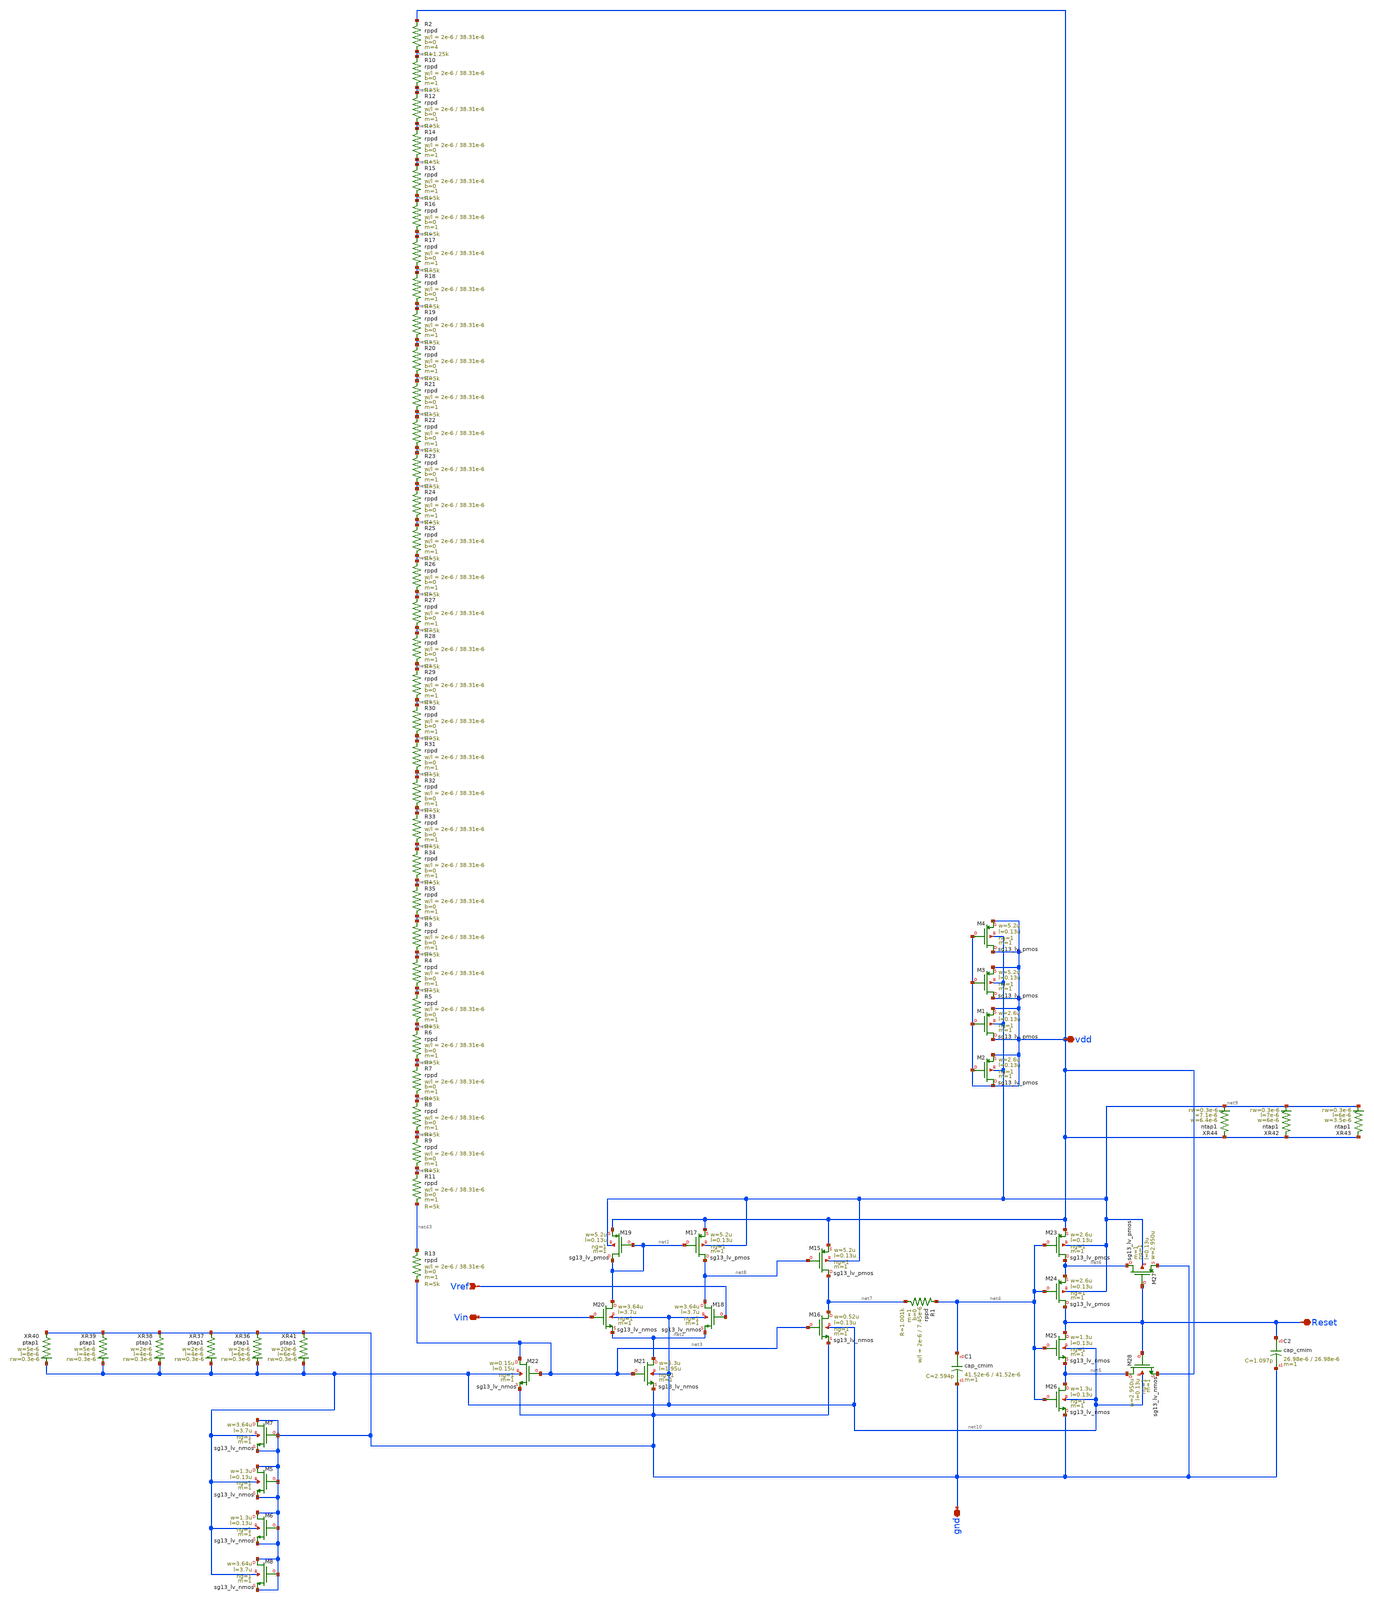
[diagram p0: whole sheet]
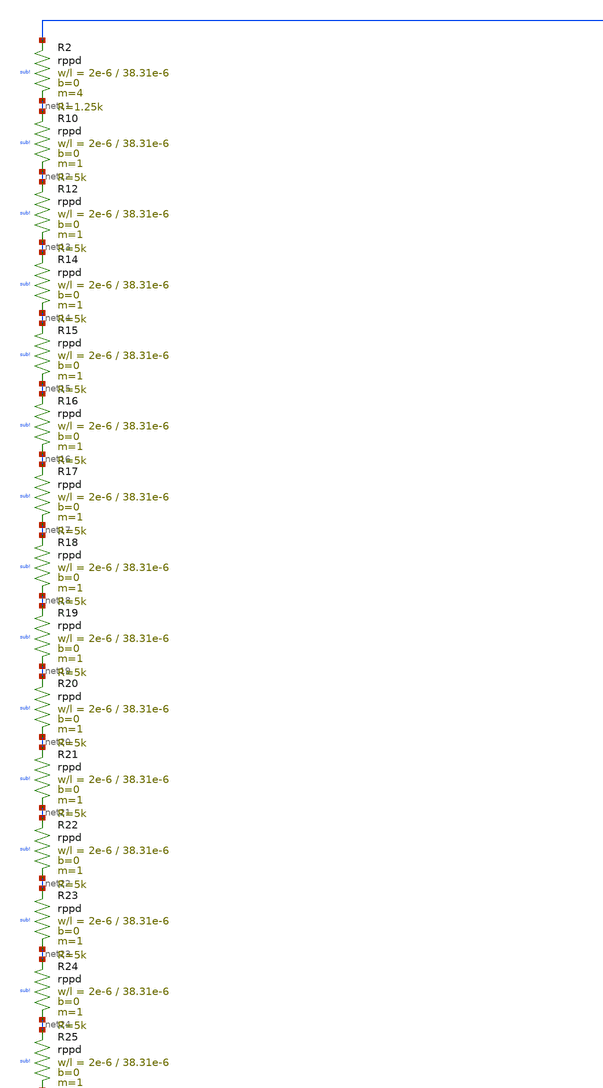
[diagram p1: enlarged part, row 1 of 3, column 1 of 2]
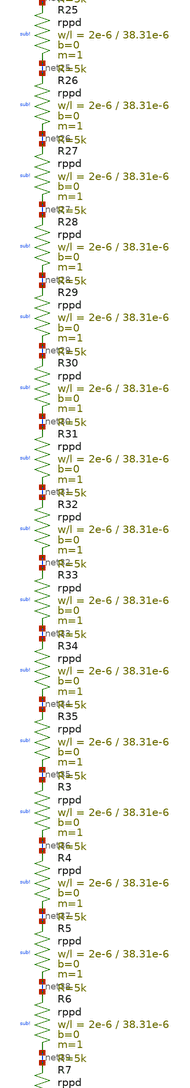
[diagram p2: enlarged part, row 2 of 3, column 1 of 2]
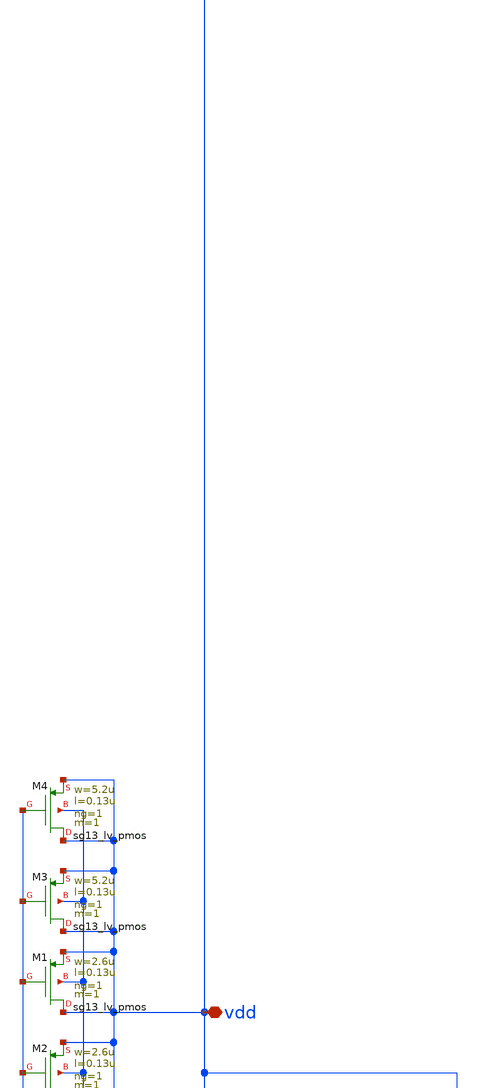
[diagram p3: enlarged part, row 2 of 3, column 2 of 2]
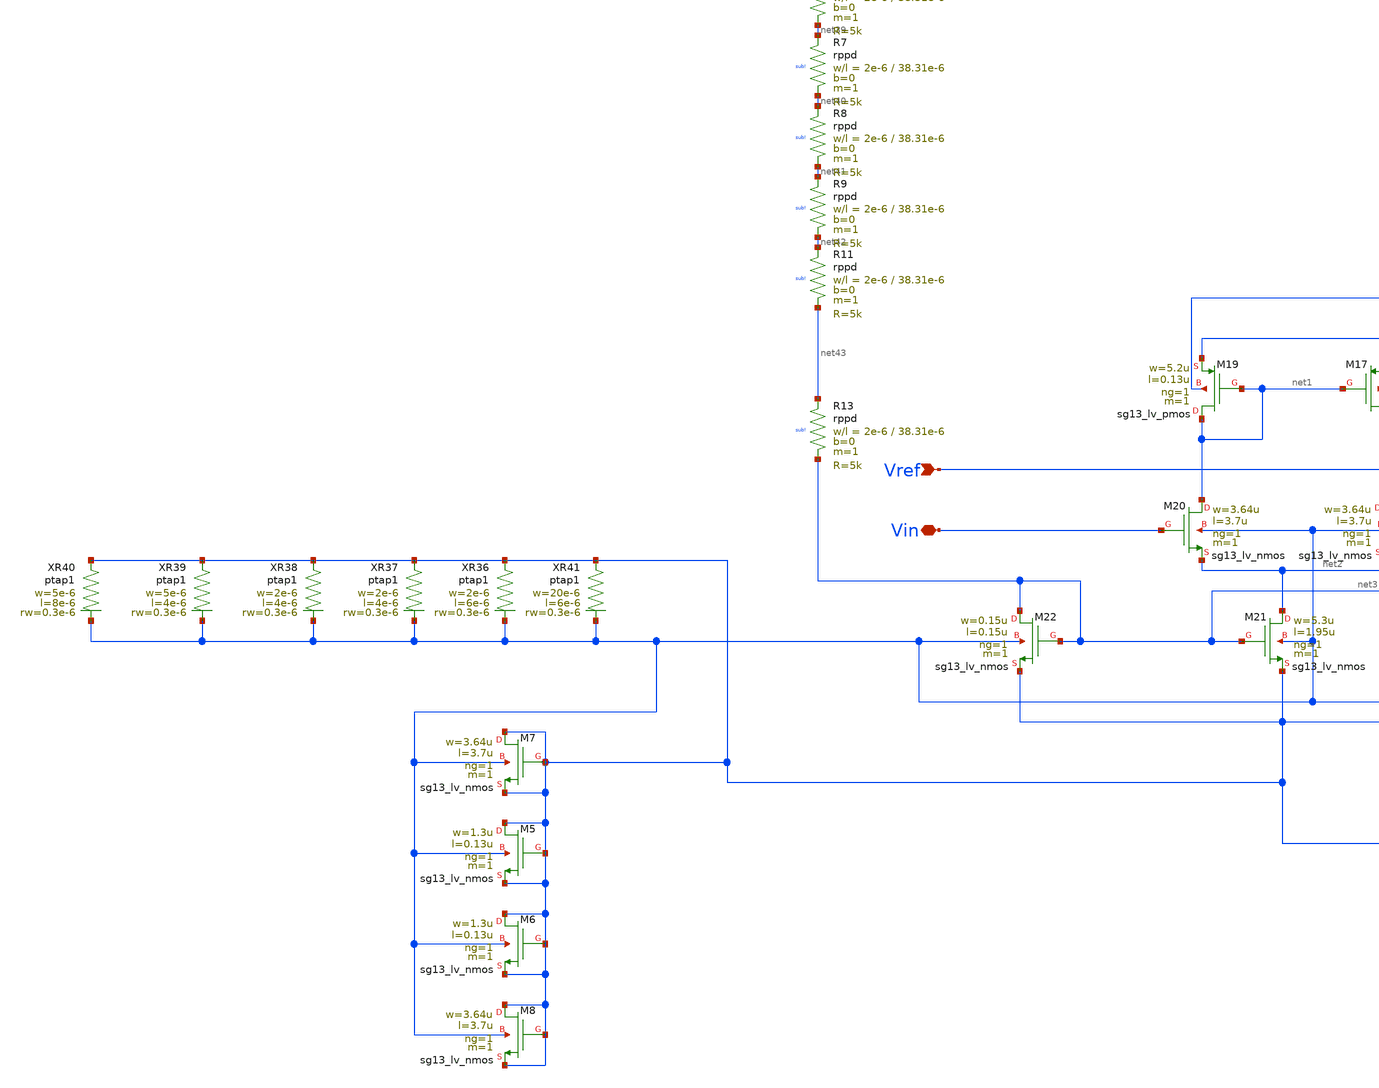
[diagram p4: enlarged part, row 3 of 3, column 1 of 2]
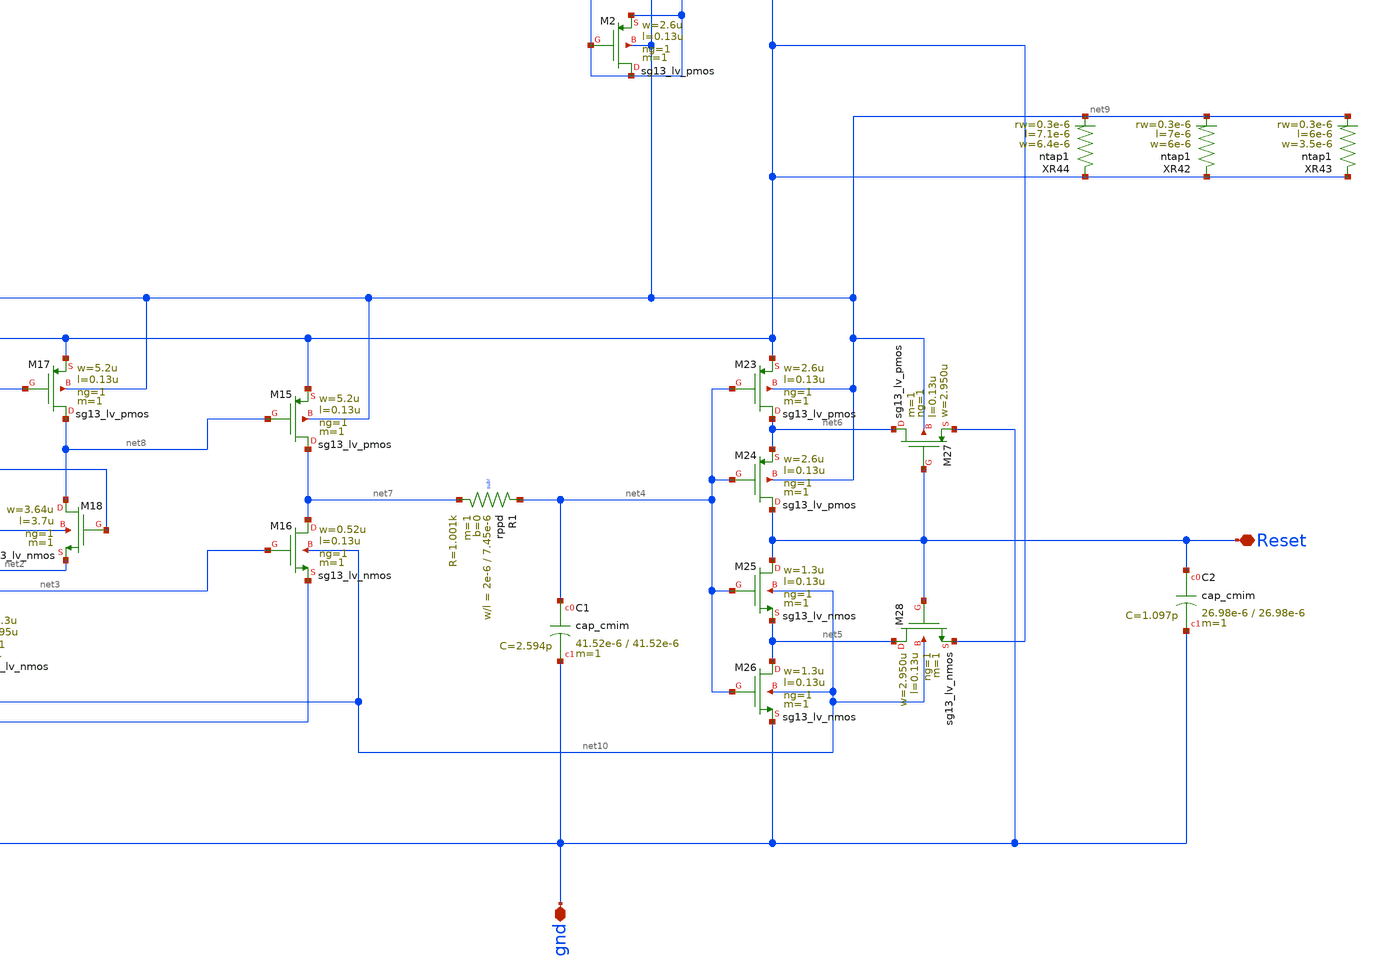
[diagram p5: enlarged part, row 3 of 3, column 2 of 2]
** sch_path: dependencies/POR/POR-main/layout/klayout/layout_POR.sch
**.subckt layout_POR Reset vdd gnd Vref Vin
*.iopin Reset
*.iopin vdd
*.iopin gnd
*.ipin Vref
*.iopin Vin
XM15 net7 net8 vdd net9 sg13_lv_pmos w=5.2u l=0.13u ng=1 m=1 mm_ok=1
XM16 net7 net3 gnd net10 sg13_lv_nmos w=0.52u l=0.13u ng=1 m=1 mm_ok=1
XM17 net8 net1 vdd net9 sg13_lv_pmos w=5.2u l=0.13u ng=1 m=1 mm_ok=1
XM18 net8 Vref net2 net10 sg13_lv_nmos w=3.64u l=3.7u ng=1 m=1 mm_ok=1
XM19 net1 net1 vdd net9 sg13_lv_pmos w=5.2u l=0.13u ng=1 m=1 mm_ok=1
XM20 net1 Vin net2 net10 sg13_lv_nmos w=3.64u l=3.7u ng=1 m=1 mm_ok=1
XM21 net2 net3 gnd net10 sg13_lv_nmos w=5.3u l=1.95u ng=1 m=1 mm_ok=1
XM22 net3 net3 gnd net10 sg13_lv_nmos w=0.15u l=0.15u ng=1 m=1 mm_ok=1
XM23 net6 net4 vdd net9 sg13_lv_pmos w=2.6u l=0.13u ng=1 m=1 mm_ok=1
XM24 Reset net4 net6 net9 sg13_lv_pmos w=2.6u l=0.13u ng=1 m=1 mm_ok=1
XM25 Reset net4 net5 net10 sg13_lv_nmos w=1.3u l=0.13u ng=1 m=1 mm_ok=1
XM26 net5 net4 gnd net10 sg13_lv_nmos w=1.3u l=0.13u ng=1 m=1 mm_ok=1
XM27 net6 Reset gnd net9 sg13_lv_pmos w=2.950u l=0.13u ng=1 m=1 mm_ok=1
XM28 net5 Reset vdd net10 sg13_lv_nmos w=2.950u l=0.13u ng=1 m=1 mm_ok=1
XC2 Reset gnd cap_cmim w=26.98e-6 l=26.98e-6 m=1 mm_ok=1
XC1 net4 gnd cap_cmim w=41.52e-6 l=41.52e-6 m=1 mm_ok=1
XM1 vdd vdd vdd net9 sg13_lv_pmos w=2.6u l=0.13u ng=1 m=1 mm_ok=1
XM2 vdd vdd vdd net9 sg13_lv_pmos w=2.6u l=0.13u ng=1 m=1 mm_ok=1
XM5 gnd gnd gnd net10 sg13_lv_nmos w=1.3u l=0.13u ng=1 m=1 mm_ok=1
XM6 gnd gnd gnd net10 sg13_lv_nmos w=1.3u l=0.13u ng=1 m=1 mm_ok=1
XM7 gnd gnd gnd net10 sg13_lv_nmos w=3.64u l=3.7u ng=1 m=1 mm_ok=1
XM8 gnd gnd gnd net10 sg13_lv_nmos w=3.64u l=3.7u ng=1 m=1 mm_ok=1
XM3 vdd vdd vdd net9 sg13_lv_pmos w=5.2u l=0.13u ng=1 m=1 mm_ok=1
XM4 vdd vdd vdd net9 sg13_lv_pmos w=5.2u l=0.13u ng=1 m=1 mm_ok=1
XR1 net4 net7 sub! rppd w=2e-6 l=7.45e-6 m=1 b=0 mm_ok=1
XR36 gnd net10 ptap1 R=15.4 w=2e-6 l=6e-6 rw=0.3e-6
XR37 gnd net10 ptap1 R=21.1 w=2e-6 l=4e-6 rw=0.3e-6
XR38 gnd net10 ptap1 R=21.1 w=2e-6 l=4e-6 rw=0.3e-6
XR39 gnd net10 ptap1 R=13.57 w=5e-6 l=4e-6 rw=0.3e-6
XR40 gnd net10 ptap1 R=9.19 w=5e-6 l=8e-6 rw=0.3e-6
XR41 gnd net10 ptap1 R=4.486 w=20e-6 l=6e-6 rw=0.3e-6
XR42 vdd net9 ntap1 R=9.19 w=6e-6 l=7e-6 rw=0.3e-6
XR43 vdd net9 ntap1 R=12.8 w=3.5e-6 l=6e-6 rw=0.3e-6
XR44 vdd net9 ntap1 R=8.834 w=6.4e-6 l=7.1e-6 rw=0.3e-6
XR2 vdd net11 sub! rppd w=2e-6 l=38.31e-6 m=4 b=0 mm_ok=1
XR10 net11 net12 sub! rppd w=2e-6 l=38.31e-6 m=1 b=0 mm_ok=1
XR12 net12 net13 sub! rppd w=2e-6 l=38.31e-6 m=1 b=0 mm_ok=1
XR14 net13 net14 sub! rppd w=2e-6 l=38.31e-6 m=1 b=0 mm_ok=1
XR15 net14 net15 sub! rppd w=2e-6 l=38.31e-6 m=1 b=0 mm_ok=1
XR16 net15 net16 sub! rppd w=2e-6 l=38.31e-6 m=1 b=0 mm_ok=1
XR17 net16 net17 sub! rppd w=2e-6 l=38.31e-6 m=1 b=0 mm_ok=1
XR18 net17 net18 sub! rppd w=2e-6 l=38.31e-6 m=1 b=0 mm_ok=1
XR19 net18 net19 sub! rppd w=2e-6 l=38.31e-6 m=1 b=0 mm_ok=1
XR20 net19 net20 sub! rppd w=2e-6 l=38.31e-6 m=1 b=0 mm_ok=1
XR21 net20 net21 sub! rppd w=2e-6 l=38.31e-6 m=1 b=0 mm_ok=1
XR22 net21 net22 sub! rppd w=2e-6 l=38.31e-6 m=1 b=0 mm_ok=1
XR23 net22 net23 sub! rppd w=2e-6 l=38.31e-6 m=1 b=0 mm_ok=1
XR24 net23 net24 sub! rppd w=2e-6 l=38.31e-6 m=1 b=0 mm_ok=1
XR25 net24 net25 sub! rppd w=2e-6 l=38.31e-6 m=1 b=0 mm_ok=1
XR26 net25 net26 sub! rppd w=2e-6 l=38.31e-6 m=1 b=0 mm_ok=1
XR27 net26 net27 sub! rppd w=2e-6 l=38.31e-6 m=1 b=0 mm_ok=1
XR28 net27 net28 sub! rppd w=2e-6 l=38.31e-6 m=1 b=0 mm_ok=1
XR29 net28 net29 sub! rppd w=2e-6 l=38.31e-6 m=1 b=0 mm_ok=1
XR30 net29 net30 sub! rppd w=2e-6 l=38.31e-6 m=1 b=0 mm_ok=1
XR31 net30 net31 sub! rppd w=2e-6 l=38.31e-6 m=1 b=0 mm_ok=1
XR32 net31 net32 sub! rppd w=2e-6 l=38.31e-6 m=1 b=0 mm_ok=1
XR33 net32 net33 sub! rppd w=2e-6 l=38.31e-6 m=1 b=0 mm_ok=1
XR34 net33 net34 sub! rppd w=2e-6 l=38.31e-6 m=1 b=0 mm_ok=1
XR35 net34 net35 sub! rppd w=2e-6 l=38.31e-6 m=1 b=0 mm_ok=1
XR3 net35 net36 sub! rppd w=2e-6 l=38.31e-6 m=1 b=0 mm_ok=1
XR4 net36 net37 sub! rppd w=2e-6 l=38.31e-6 m=1 b=0 mm_ok=1
XR5 net37 net38 sub! rppd w=2e-6 l=38.31e-6 m=1 b=0 mm_ok=1
XR6 net38 net39 sub! rppd w=2e-6 l=38.31e-6 m=1 b=0 mm_ok=1
XR7 net39 net40 sub! rppd w=2e-6 l=38.31e-6 m=1 b=0 mm_ok=1
XR8 net40 net41 sub! rppd w=2e-6 l=38.31e-6 m=1 b=0 mm_ok=1
XR9 net41 net42 sub! rppd w=2e-6 l=38.31e-6 m=1 b=0 mm_ok=1
XR11 net42 net43 sub! rppd w=2e-6 l=38.31e-6 m=1 b=0 mm_ok=1
XR13 net43 net3 sub! rppd w=2e-6 l=38.31e-6 m=1 b=0 mm_ok=1
**.ends
.end
